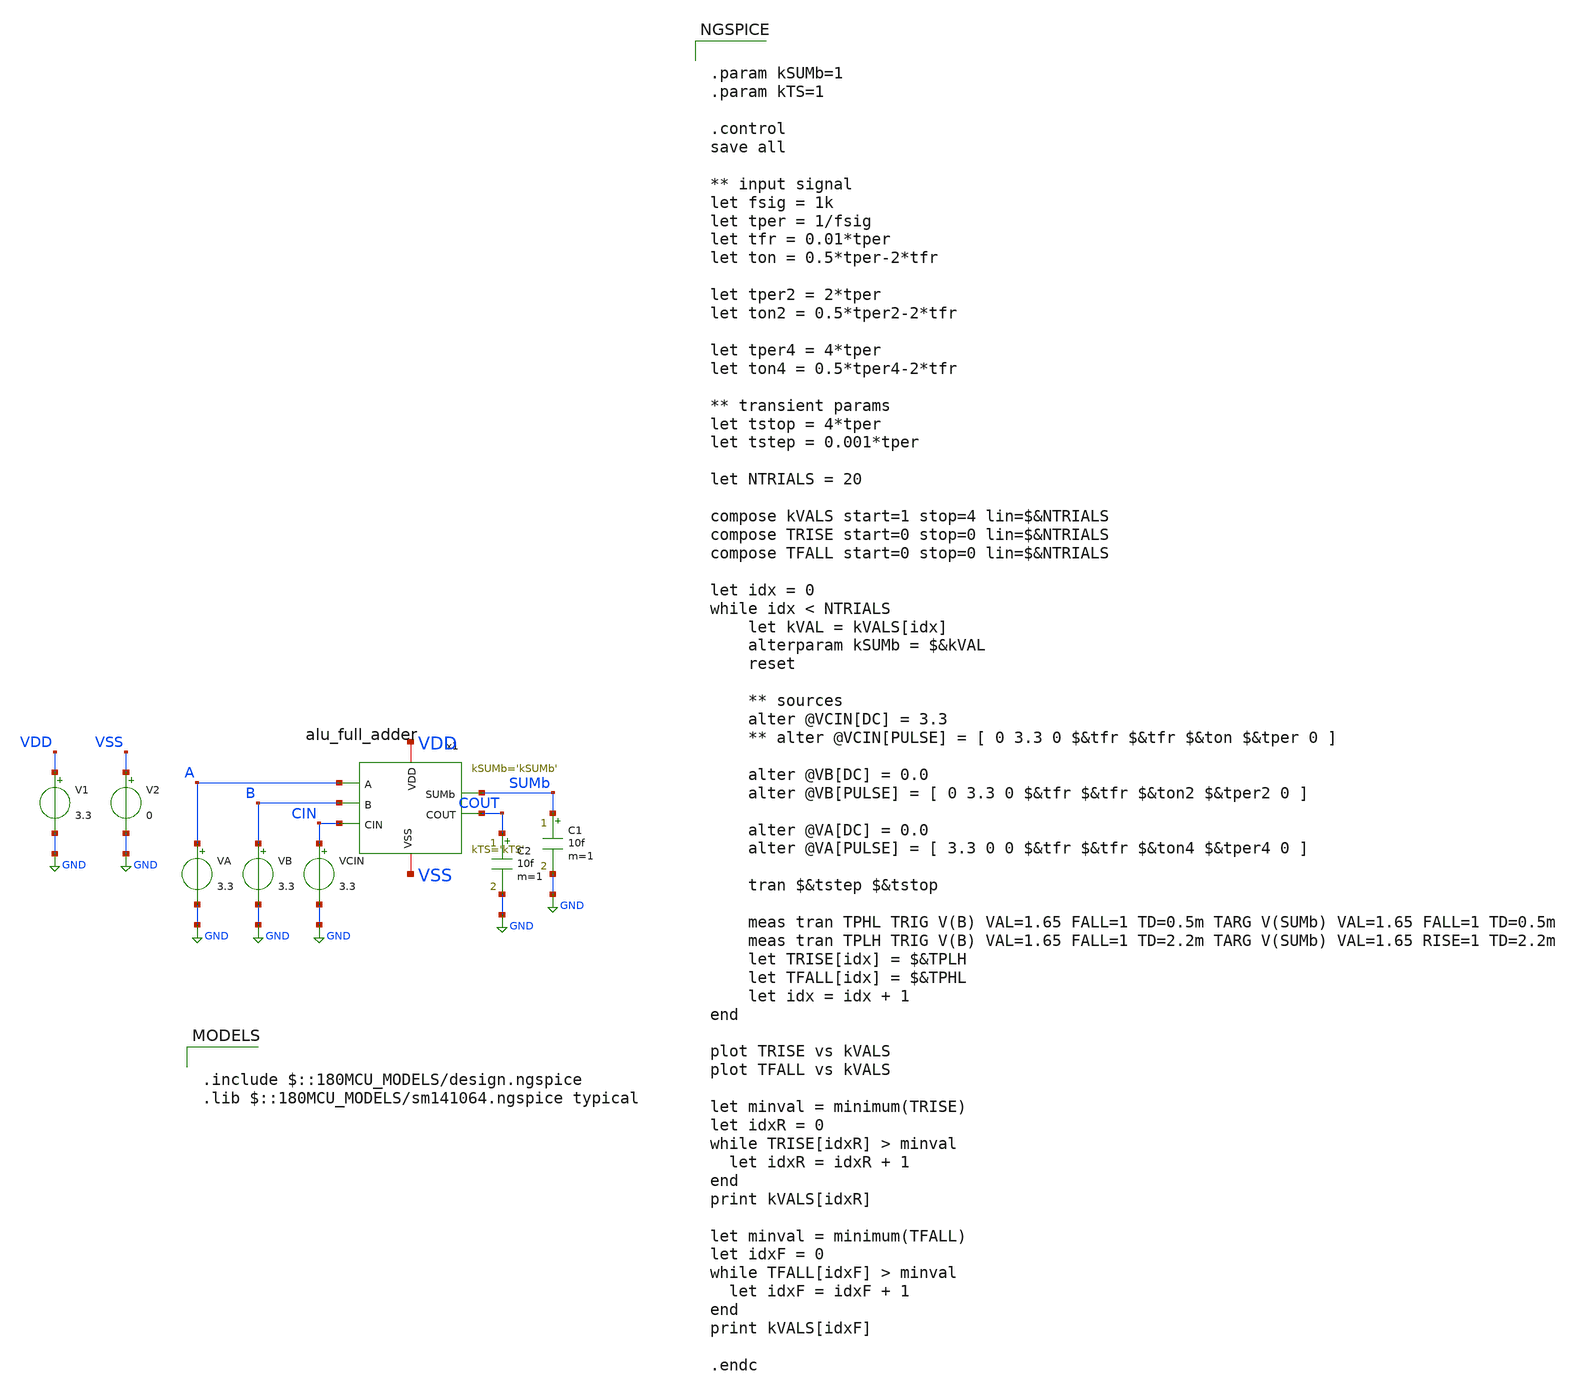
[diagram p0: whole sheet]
** sch_path: CAD4/full_adder_sizing_tb.sch
**.subckt full_adder_sizing_tb
V1 VDD GND 3.3
VA A GND 3.3
VB B GND 3.3
VCIN CIN GND 3.3
C1 SUMb GND 10f m=1
V2 VSS GND 0
x1 VDD VSS A B CIN SUMb COUT alu_full_adder kSUMb='kSUMb' kTS='kTS'
C2 COUT GND 10f m=1
**** begin user architecture code

.include $::180MCU_MODELS/design.ngspice
.lib $::180MCU_MODELS/sm141064.ngspice typical



.param kSUMb=1
.param kTS=1

.control
save all

** input signal
let fsig = 1k
let tper = 1/fsig
let tfr = 0.01*tper
let ton = 0.5*tper-2*tfr

let tper2 = 2*tper
let ton2 = 0.5*tper2-2*tfr

let tper4 = 4*tper
let ton4 = 0.5*tper4-2*tfr

** transient params
let tstop = 4*tper
let tstep = 0.001*tper

let NTRIALS = 20

compose kVALS start=1 stop=4 lin=$&NTRIALS
compose TRISE start=0 stop=0 lin=$&NTRIALS
compose TFALL start=0 stop=0 lin=$&NTRIALS

let idx = 0
while idx < NTRIALS
	let kVAL = kVALS[idx]
	alterparam kSUMb = $&kVAL
	reset

	** sources
	alter @VCIN[DC] = 3.3
	** alter @VCIN[PULSE] = [ 0 3.3 0 $&tfr $&tfr $&ton $&tper 0 ]

	alter @VB[DC] = 0.0
	alter @VB[PULSE] = [ 0 3.3 0 $&tfr $&tfr $&ton2 $&tper2 0 ]

	alter @VA[DC] = 0.0
	alter @VA[PULSE] = [ 3.3 0 0 $&tfr $&tfr $&ton4 $&tper4 0 ]

	tran $&tstep $&tstop

	meas tran TPHL TRIG V(B) VAL=1.65 FALL=1 TD=0.5m TARG V(SUMb) VAL=1.65 FALL=1 TD=0.5m
	meas tran TPLH TRIG V(B) VAL=1.65 FALL=1 TD=2.2m TARG V(SUMb) VAL=1.65 RISE=1 TD=2.2m
	let TRISE[idx] = $&TPLH
	let TFALL[idx] = $&TPHL
	let idx = idx + 1
end

plot TRISE vs kVALS
plot TFALL vs kVALS

let minval = minimum(TRISE)
let idxR = 0
while TRISE[idxR] > minval
  let idxR = idxR + 1
end
print kVALS[idxR]

let minval = minimum(TFALL)
let idxF = 0
while TFALL[idxF] > minval
  let idxF = idxF + 1
end
print kVALS[idxF]

.endc


**** end user architecture code
**.ends
.GLOBAL GND
.end
